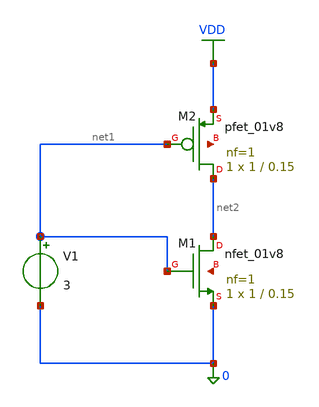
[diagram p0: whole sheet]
** sch_path: stage0/inverter/inverter.sch
**.subckt inverter
XM1 net2 net1 0 net3 sky130_fd_pr__nfet_01v8 L=0.15 W=1 nf=1 ad='int((1 + 1)/2) * 1 / 1 * 0.29' as='int((1 + 2)/2) * 1 / 1 * 0.29'
+ pd='2*int((1 + 1)/2) * (1 / 1 + 0.29)' ps='2*int((1 + 2)/2) * (1 / 1 + 0.29)' nrd='0.29 / 1 ' nrs='0.29 / 1 '
+ sa=0 sb=0 sd=0 mult=1 m=1
XM2 net2 net1 VDD net4 sky130_fd_pr__pfet_01v8 L=0.15 W=1 nf=1 ad='int((1 + 1)/2) * 1 / 1 * 0.29' as='int((1 + 2)/2) * 1 / 1 * 0.29'
+ pd='2*int((1 + 1)/2) * (1 / 1 + 0.29)' ps='2*int((1 + 2)/2) * (1 / 1 + 0.29)' nrd='0.29 / 1 ' nrs='0.29 / 1 '
+ sa=0 sb=0 sd=0 mult=1 m=1
V1 net1 0 3
**.ends
.GLOBAL VDD
.end
